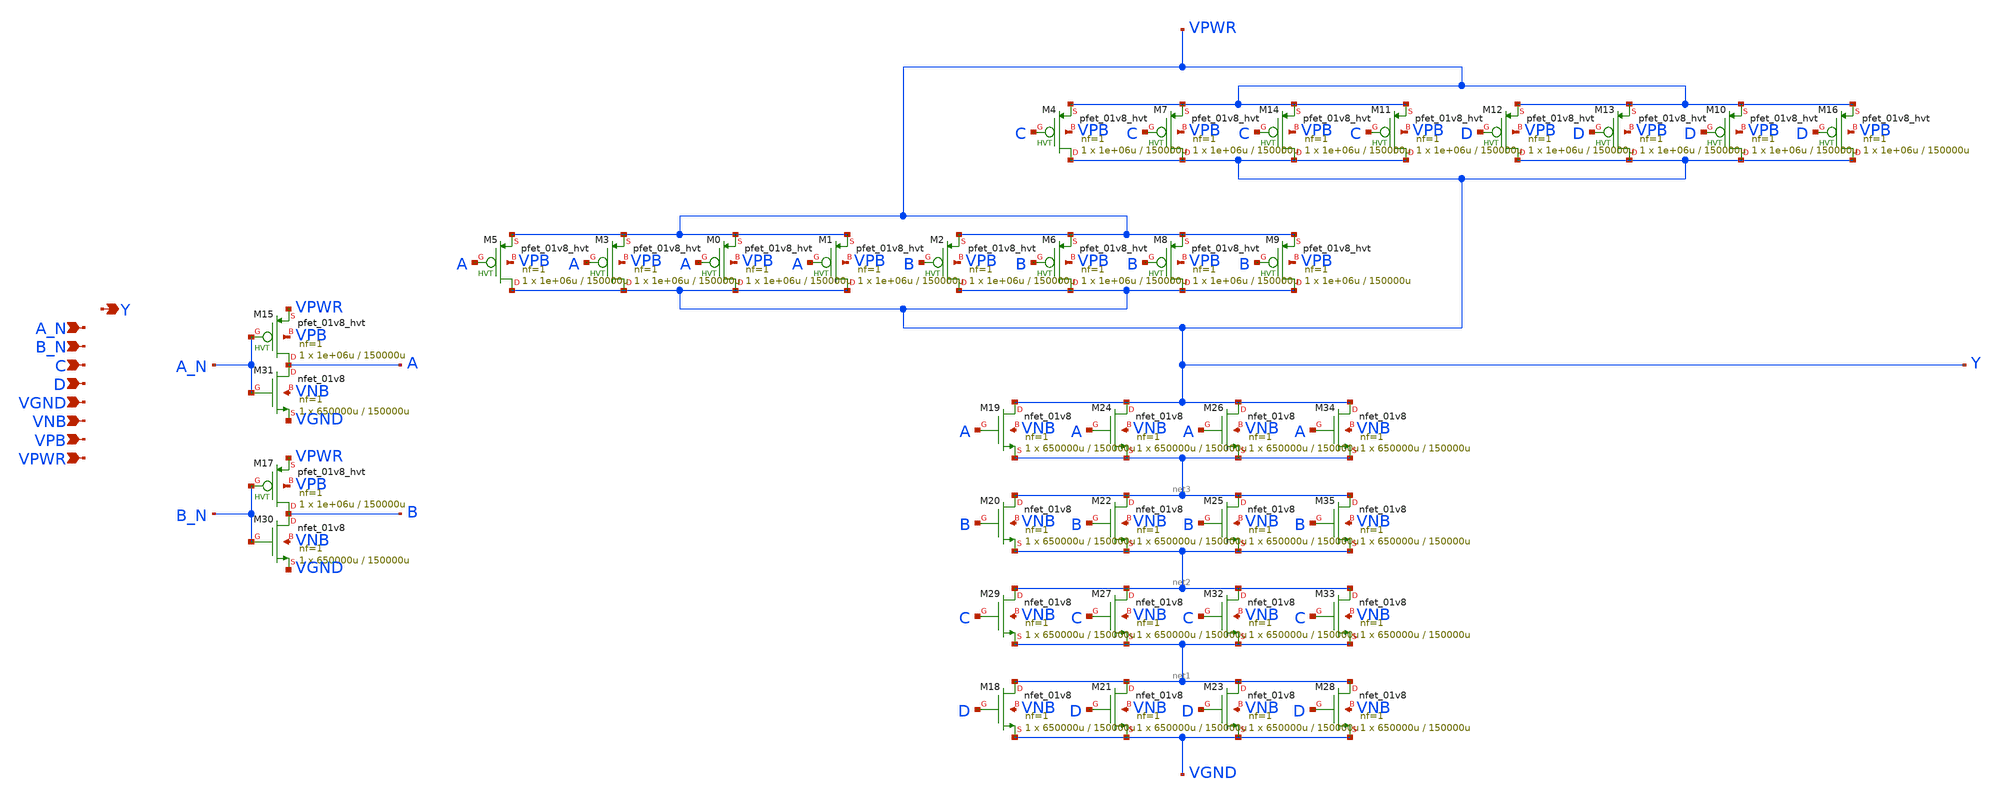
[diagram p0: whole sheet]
** sch_path: schematics/nand4bb/sky130_fd_sc_hd__nand4bb_4.sch
**.subckt sky130_fd_sc_hd__nand4bb_4 A_N B_N C D VGND VNB VPB VPWR Y
*.ipin A_N
*.ipin B_N
*.ipin C
*.ipin D
*.ipin VGND
*.ipin VNB
*.ipin VPB
*.ipin VPWR
*.opin Y
XM0 Y A VPWR VPB sky130_fd_pr__pfet_01v8_hvt L=150000u W=1e+06u nf=1 ad='int((1 + 1)/2) * 1e+06u / 1 * 0.29'
+ as='int((1 + 2)/2) * 1e+06u / 1 * 0.29' pd='2*int((1 + 1)/2) * (1e+06u / 1 + 0.29)' ps='2*int((1 + 2)/2) * (1e+06u / 1 + 0.29)'
+ nrd='0.29 / 1e+06u ' nrs='0.29 / 1e+06u ' sa=0 sb=0 sd=0 mult=1 m=1
XM1 Y A VPWR VPB sky130_fd_pr__pfet_01v8_hvt L=150000u W=1e+06u nf=1 ad='int((1 + 1)/2) * 1e+06u / 1 * 0.29'
+ as='int((1 + 2)/2) * 1e+06u / 1 * 0.29' pd='2*int((1 + 1)/2) * (1e+06u / 1 + 0.29)' ps='2*int((1 + 2)/2) * (1e+06u / 1 + 0.29)'
+ nrd='0.29 / 1e+06u ' nrs='0.29 / 1e+06u ' sa=0 sb=0 sd=0 mult=1 m=1
XM2 Y B VPWR VPB sky130_fd_pr__pfet_01v8_hvt L=150000u W=1e+06u nf=1 ad='int((1 + 1)/2) * 1e+06u / 1 * 0.29'
+ as='int((1 + 2)/2) * 1e+06u / 1 * 0.29' pd='2*int((1 + 1)/2) * (1e+06u / 1 + 0.29)' ps='2*int((1 + 2)/2) * (1e+06u / 1 + 0.29)'
+ nrd='0.29 / 1e+06u ' nrs='0.29 / 1e+06u ' sa=0 sb=0 sd=0 mult=1 m=1
XM3 Y A VPWR VPB sky130_fd_pr__pfet_01v8_hvt L=150000u W=1e+06u nf=1 ad='int((1 + 1)/2) * 1e+06u / 1 * 0.29'
+ as='int((1 + 2)/2) * 1e+06u / 1 * 0.29' pd='2*int((1 + 1)/2) * (1e+06u / 1 + 0.29)' ps='2*int((1 + 2)/2) * (1e+06u / 1 + 0.29)'
+ nrd='0.29 / 1e+06u ' nrs='0.29 / 1e+06u ' sa=0 sb=0 sd=0 mult=1 m=1
XM4 Y C VPWR VPB sky130_fd_pr__pfet_01v8_hvt L=150000u W=1e+06u nf=1 ad='int((1 + 1)/2) * 1e+06u / 1 * 0.29'
+ as='int((1 + 2)/2) * 1e+06u / 1 * 0.29' pd='2*int((1 + 1)/2) * (1e+06u / 1 + 0.29)' ps='2*int((1 + 2)/2) * (1e+06u / 1 + 0.29)'
+ nrd='0.29 / 1e+06u ' nrs='0.29 / 1e+06u ' sa=0 sb=0 sd=0 mult=1 m=1
XM5 Y A VPWR VPB sky130_fd_pr__pfet_01v8_hvt L=150000u W=1e+06u nf=1 ad='int((1 + 1)/2) * 1e+06u / 1 * 0.29'
+ as='int((1 + 2)/2) * 1e+06u / 1 * 0.29' pd='2*int((1 + 1)/2) * (1e+06u / 1 + 0.29)' ps='2*int((1 + 2)/2) * (1e+06u / 1 + 0.29)'
+ nrd='0.29 / 1e+06u ' nrs='0.29 / 1e+06u ' sa=0 sb=0 sd=0 mult=1 m=1
XM6 Y B VPWR VPB sky130_fd_pr__pfet_01v8_hvt L=150000u W=1e+06u nf=1 ad='int((1 + 1)/2) * 1e+06u / 1 * 0.29'
+ as='int((1 + 2)/2) * 1e+06u / 1 * 0.29' pd='2*int((1 + 1)/2) * (1e+06u / 1 + 0.29)' ps='2*int((1 + 2)/2) * (1e+06u / 1 + 0.29)'
+ nrd='0.29 / 1e+06u ' nrs='0.29 / 1e+06u ' sa=0 sb=0 sd=0 mult=1 m=1
XM7 Y C VPWR VPB sky130_fd_pr__pfet_01v8_hvt L=150000u W=1e+06u nf=1 ad='int((1 + 1)/2) * 1e+06u / 1 * 0.29'
+ as='int((1 + 2)/2) * 1e+06u / 1 * 0.29' pd='2*int((1 + 1)/2) * (1e+06u / 1 + 0.29)' ps='2*int((1 + 2)/2) * (1e+06u / 1 + 0.29)'
+ nrd='0.29 / 1e+06u ' nrs='0.29 / 1e+06u ' sa=0 sb=0 sd=0 mult=1 m=1
XM8 Y B VPWR VPB sky130_fd_pr__pfet_01v8_hvt L=150000u W=1e+06u nf=1 ad='int((1 + 1)/2) * 1e+06u / 1 * 0.29'
+ as='int((1 + 2)/2) * 1e+06u / 1 * 0.29' pd='2*int((1 + 1)/2) * (1e+06u / 1 + 0.29)' ps='2*int((1 + 2)/2) * (1e+06u / 1 + 0.29)'
+ nrd='0.29 / 1e+06u ' nrs='0.29 / 1e+06u ' sa=0 sb=0 sd=0 mult=1 m=1
XM9 Y B VPWR VPB sky130_fd_pr__pfet_01v8_hvt L=150000u W=1e+06u nf=1 ad='int((1 + 1)/2) * 1e+06u / 1 * 0.29'
+ as='int((1 + 2)/2) * 1e+06u / 1 * 0.29' pd='2*int((1 + 1)/2) * (1e+06u / 1 + 0.29)' ps='2*int((1 + 2)/2) * (1e+06u / 1 + 0.29)'
+ nrd='0.29 / 1e+06u ' nrs='0.29 / 1e+06u ' sa=0 sb=0 sd=0 mult=1 m=1
XM10 Y D VPWR VPB sky130_fd_pr__pfet_01v8_hvt L=150000u W=1e+06u nf=1 ad='int((1 + 1)/2) * 1e+06u / 1 * 0.29'
+ as='int((1 + 2)/2) * 1e+06u / 1 * 0.29' pd='2*int((1 + 1)/2) * (1e+06u / 1 + 0.29)' ps='2*int((1 + 2)/2) * (1e+06u / 1 + 0.29)'
+ nrd='0.29 / 1e+06u ' nrs='0.29 / 1e+06u ' sa=0 sb=0 sd=0 mult=1 m=1
XM11 Y C VPWR VPB sky130_fd_pr__pfet_01v8_hvt L=150000u W=1e+06u nf=1 ad='int((1 + 1)/2) * 1e+06u / 1 * 0.29'
+ as='int((1 + 2)/2) * 1e+06u / 1 * 0.29' pd='2*int((1 + 1)/2) * (1e+06u / 1 + 0.29)' ps='2*int((1 + 2)/2) * (1e+06u / 1 + 0.29)'
+ nrd='0.29 / 1e+06u ' nrs='0.29 / 1e+06u ' sa=0 sb=0 sd=0 mult=1 m=1
XM12 Y D VPWR VPB sky130_fd_pr__pfet_01v8_hvt L=150000u W=1e+06u nf=1 ad='int((1 + 1)/2) * 1e+06u / 1 * 0.29'
+ as='int((1 + 2)/2) * 1e+06u / 1 * 0.29' pd='2*int((1 + 1)/2) * (1e+06u / 1 + 0.29)' ps='2*int((1 + 2)/2) * (1e+06u / 1 + 0.29)'
+ nrd='0.29 / 1e+06u ' nrs='0.29 / 1e+06u ' sa=0 sb=0 sd=0 mult=1 m=1
XM13 Y D VPWR VPB sky130_fd_pr__pfet_01v8_hvt L=150000u W=1e+06u nf=1 ad='int((1 + 1)/2) * 1e+06u / 1 * 0.29'
+ as='int((1 + 2)/2) * 1e+06u / 1 * 0.29' pd='2*int((1 + 1)/2) * (1e+06u / 1 + 0.29)' ps='2*int((1 + 2)/2) * (1e+06u / 1 + 0.29)'
+ nrd='0.29 / 1e+06u ' nrs='0.29 / 1e+06u ' sa=0 sb=0 sd=0 mult=1 m=1
XM14 Y C VPWR VPB sky130_fd_pr__pfet_01v8_hvt L=150000u W=1e+06u nf=1 ad='int((1 + 1)/2) * 1e+06u / 1 * 0.29'
+ as='int((1 + 2)/2) * 1e+06u / 1 * 0.29' pd='2*int((1 + 1)/2) * (1e+06u / 1 + 0.29)' ps='2*int((1 + 2)/2) * (1e+06u / 1 + 0.29)'
+ nrd='0.29 / 1e+06u ' nrs='0.29 / 1e+06u ' sa=0 sb=0 sd=0 mult=1 m=1
XM16 Y D VPWR VPB sky130_fd_pr__pfet_01v8_hvt L=150000u W=1e+06u nf=1 ad='int((1 + 1)/2) * 1e+06u / 1 * 0.29'
+ as='int((1 + 2)/2) * 1e+06u / 1 * 0.29' pd='2*int((1 + 1)/2) * (1e+06u / 1 + 0.29)' ps='2*int((1 + 2)/2) * (1e+06u / 1 + 0.29)'
+ nrd='0.29 / 1e+06u ' nrs='0.29 / 1e+06u ' sa=0 sb=0 sd=0 mult=1 m=1
XM18 net1 D VGND VNB sky130_fd_pr__nfet_01v8 L=150000u W=650000u nf=1 ad='int((1 + 1)/2) * 650000u / 1 * 0.29'
+ as='int((1 + 2)/2) * 650000u / 1 * 0.29' pd='2*int((1 + 1)/2) * (650000u / 1 + 0.29)' ps='2*int((1 + 2)/2) * (650000u / 1 + 0.29)'
+ nrd='0.29 / 650000u ' nrs='0.29 / 650000u ' sa=0 sb=0 sd=0 mult=1 m=1
XM19 Y A net3 VNB sky130_fd_pr__nfet_01v8 L=150000u W=650000u nf=1 ad='int((1 + 1)/2) * 650000u / 1 * 0.29'
+ as='int((1 + 2)/2) * 650000u / 1 * 0.29' pd='2*int((1 + 1)/2) * (650000u / 1 + 0.29)' ps='2*int((1 + 2)/2) * (650000u / 1 + 0.29)'
+ nrd='0.29 / 650000u ' nrs='0.29 / 650000u ' sa=0 sb=0 sd=0 mult=1 m=1
XM20 net3 B net2 VNB sky130_fd_pr__nfet_01v8 L=150000u W=650000u nf=1 ad='int((1 + 1)/2) * 650000u / 1 * 0.29'
+ as='int((1 + 2)/2) * 650000u / 1 * 0.29' pd='2*int((1 + 1)/2) * (650000u / 1 + 0.29)' ps='2*int((1 + 2)/2) * (650000u / 1 + 0.29)'
+ nrd='0.29 / 650000u ' nrs='0.29 / 650000u ' sa=0 sb=0 sd=0 mult=1 m=1
XM21 net1 D VGND VNB sky130_fd_pr__nfet_01v8 L=150000u W=650000u nf=1 ad='int((1 + 1)/2) * 650000u / 1 * 0.29'
+ as='int((1 + 2)/2) * 650000u / 1 * 0.29' pd='2*int((1 + 1)/2) * (650000u / 1 + 0.29)' ps='2*int((1 + 2)/2) * (650000u / 1 + 0.29)'
+ nrd='0.29 / 650000u ' nrs='0.29 / 650000u ' sa=0 sb=0 sd=0 mult=1 m=1
XM22 net3 B net2 VNB sky130_fd_pr__nfet_01v8 L=150000u W=650000u nf=1 ad='int((1 + 1)/2) * 650000u / 1 * 0.29'
+ as='int((1 + 2)/2) * 650000u / 1 * 0.29' pd='2*int((1 + 1)/2) * (650000u / 1 + 0.29)' ps='2*int((1 + 2)/2) * (650000u / 1 + 0.29)'
+ nrd='0.29 / 650000u ' nrs='0.29 / 650000u ' sa=0 sb=0 sd=0 mult=1 m=1
XM23 net1 D VGND VNB sky130_fd_pr__nfet_01v8 L=150000u W=650000u nf=1 ad='int((1 + 1)/2) * 650000u / 1 * 0.29'
+ as='int((1 + 2)/2) * 650000u / 1 * 0.29' pd='2*int((1 + 1)/2) * (650000u / 1 + 0.29)' ps='2*int((1 + 2)/2) * (650000u / 1 + 0.29)'
+ nrd='0.29 / 650000u ' nrs='0.29 / 650000u ' sa=0 sb=0 sd=0 mult=1 m=1
XM24 Y A net3 VNB sky130_fd_pr__nfet_01v8 L=150000u W=650000u nf=1 ad='int((1 + 1)/2) * 650000u / 1 * 0.29'
+ as='int((1 + 2)/2) * 650000u / 1 * 0.29' pd='2*int((1 + 1)/2) * (650000u / 1 + 0.29)' ps='2*int((1 + 2)/2) * (650000u / 1 + 0.29)'
+ nrd='0.29 / 650000u ' nrs='0.29 / 650000u ' sa=0 sb=0 sd=0 mult=1 m=1
XM25 net3 B net2 VNB sky130_fd_pr__nfet_01v8 L=150000u W=650000u nf=1 ad='int((1 + 1)/2) * 650000u / 1 * 0.29'
+ as='int((1 + 2)/2) * 650000u / 1 * 0.29' pd='2*int((1 + 1)/2) * (650000u / 1 + 0.29)' ps='2*int((1 + 2)/2) * (650000u / 1 + 0.29)'
+ nrd='0.29 / 650000u ' nrs='0.29 / 650000u ' sa=0 sb=0 sd=0 mult=1 m=1
XM26 Y A net3 VNB sky130_fd_pr__nfet_01v8 L=150000u W=650000u nf=1 ad='int((1 + 1)/2) * 650000u / 1 * 0.29'
+ as='int((1 + 2)/2) * 650000u / 1 * 0.29' pd='2*int((1 + 1)/2) * (650000u / 1 + 0.29)' ps='2*int((1 + 2)/2) * (650000u / 1 + 0.29)'
+ nrd='0.29 / 650000u ' nrs='0.29 / 650000u ' sa=0 sb=0 sd=0 mult=1 m=1
XM27 net2 C net1 VNB sky130_fd_pr__nfet_01v8 L=150000u W=650000u nf=1 ad='int((1 + 1)/2) * 650000u / 1 * 0.29'
+ as='int((1 + 2)/2) * 650000u / 1 * 0.29' pd='2*int((1 + 1)/2) * (650000u / 1 + 0.29)' ps='2*int((1 + 2)/2) * (650000u / 1 + 0.29)'
+ nrd='0.29 / 650000u ' nrs='0.29 / 650000u ' sa=0 sb=0 sd=0 mult=1 m=1
XM28 net1 D VGND VNB sky130_fd_pr__nfet_01v8 L=150000u W=650000u nf=1 ad='int((1 + 1)/2) * 650000u / 1 * 0.29'
+ as='int((1 + 2)/2) * 650000u / 1 * 0.29' pd='2*int((1 + 1)/2) * (650000u / 1 + 0.29)' ps='2*int((1 + 2)/2) * (650000u / 1 + 0.29)'
+ nrd='0.29 / 650000u ' nrs='0.29 / 650000u ' sa=0 sb=0 sd=0 mult=1 m=1
XM29 net2 C net1 VNB sky130_fd_pr__nfet_01v8 L=150000u W=650000u nf=1 ad='int((1 + 1)/2) * 650000u / 1 * 0.29'
+ as='int((1 + 2)/2) * 650000u / 1 * 0.29' pd='2*int((1 + 1)/2) * (650000u / 1 + 0.29)' ps='2*int((1 + 2)/2) * (650000u / 1 + 0.29)'
+ nrd='0.29 / 650000u ' nrs='0.29 / 650000u ' sa=0 sb=0 sd=0 mult=1 m=1
XM32 net2 C net1 VNB sky130_fd_pr__nfet_01v8 L=150000u W=650000u nf=1 ad='int((1 + 1)/2) * 650000u / 1 * 0.29'
+ as='int((1 + 2)/2) * 650000u / 1 * 0.29' pd='2*int((1 + 1)/2) * (650000u / 1 + 0.29)' ps='2*int((1 + 2)/2) * (650000u / 1 + 0.29)'
+ nrd='0.29 / 650000u ' nrs='0.29 / 650000u ' sa=0 sb=0 sd=0 mult=1 m=1
XM33 net2 C net1 VNB sky130_fd_pr__nfet_01v8 L=150000u W=650000u nf=1 ad='int((1 + 1)/2) * 650000u / 1 * 0.29'
+ as='int((1 + 2)/2) * 650000u / 1 * 0.29' pd='2*int((1 + 1)/2) * (650000u / 1 + 0.29)' ps='2*int((1 + 2)/2) * (650000u / 1 + 0.29)'
+ nrd='0.29 / 650000u ' nrs='0.29 / 650000u ' sa=0 sb=0 sd=0 mult=1 m=1
XM34 Y A net3 VNB sky130_fd_pr__nfet_01v8 L=150000u W=650000u nf=1 ad='int((1 + 1)/2) * 650000u / 1 * 0.29'
+ as='int((1 + 2)/2) * 650000u / 1 * 0.29' pd='2*int((1 + 1)/2) * (650000u / 1 + 0.29)' ps='2*int((1 + 2)/2) * (650000u / 1 + 0.29)'
+ nrd='0.29 / 650000u ' nrs='0.29 / 650000u ' sa=0 sb=0 sd=0 mult=1 m=1
XM35 net3 B net2 VNB sky130_fd_pr__nfet_01v8 L=150000u W=650000u nf=1 ad='int((1 + 1)/2) * 650000u / 1 * 0.29'
+ as='int((1 + 2)/2) * 650000u / 1 * 0.29' pd='2*int((1 + 1)/2) * (650000u / 1 + 0.29)' ps='2*int((1 + 2)/2) * (650000u / 1 + 0.29)'
+ nrd='0.29 / 650000u ' nrs='0.29 / 650000u ' sa=0 sb=0 sd=0 mult=1 m=1
XM15 A A_N VPWR VPB sky130_fd_pr__pfet_01v8_hvt L=150000u W=1e+06u nf=1 ad='int((1 + 1)/2) * 1e+06u / 1 * 0.29'
+ as='int((1 + 2)/2) * 1e+06u / 1 * 0.29' pd='2*int((1 + 1)/2) * (1e+06u / 1 + 0.29)' ps='2*int((1 + 2)/2) * (1e+06u / 1 + 0.29)'
+ nrd='0.29 / 1e+06u ' nrs='0.29 / 1e+06u ' sa=0 sb=0 sd=0 mult=1 m=1
XM17 B B_N VPWR VPB sky130_fd_pr__pfet_01v8_hvt L=150000u W=1e+06u nf=1 ad='int((1 + 1)/2) * 1e+06u / 1 * 0.29'
+ as='int((1 + 2)/2) * 1e+06u / 1 * 0.29' pd='2*int((1 + 1)/2) * (1e+06u / 1 + 0.29)' ps='2*int((1 + 2)/2) * (1e+06u / 1 + 0.29)'
+ nrd='0.29 / 1e+06u ' nrs='0.29 / 1e+06u ' sa=0 sb=0 sd=0 mult=1 m=1
XM31 A A_N VGND VNB sky130_fd_pr__nfet_01v8 L=150000u W=650000u nf=1 ad='int((1 + 1)/2) * 650000u / 1 * 0.29'
+ as='int((1 + 2)/2) * 650000u / 1 * 0.29' pd='2*int((1 + 1)/2) * (650000u / 1 + 0.29)' ps='2*int((1 + 2)/2) * (650000u / 1 + 0.29)'
+ nrd='0.29 / 650000u ' nrs='0.29 / 650000u ' sa=0 sb=0 sd=0 mult=1 m=1
XM30 B B_N VGND VNB sky130_fd_pr__nfet_01v8 L=150000u W=650000u nf=1 ad='int((1 + 1)/2) * 650000u / 1 * 0.29'
+ as='int((1 + 2)/2) * 650000u / 1 * 0.29' pd='2*int((1 + 1)/2) * (650000u / 1 + 0.29)' ps='2*int((1 + 2)/2) * (650000u / 1 + 0.29)'
+ nrd='0.29 / 650000u ' nrs='0.29 / 650000u ' sa=0 sb=0 sd=0 mult=1 m=1
**.ends
.end
